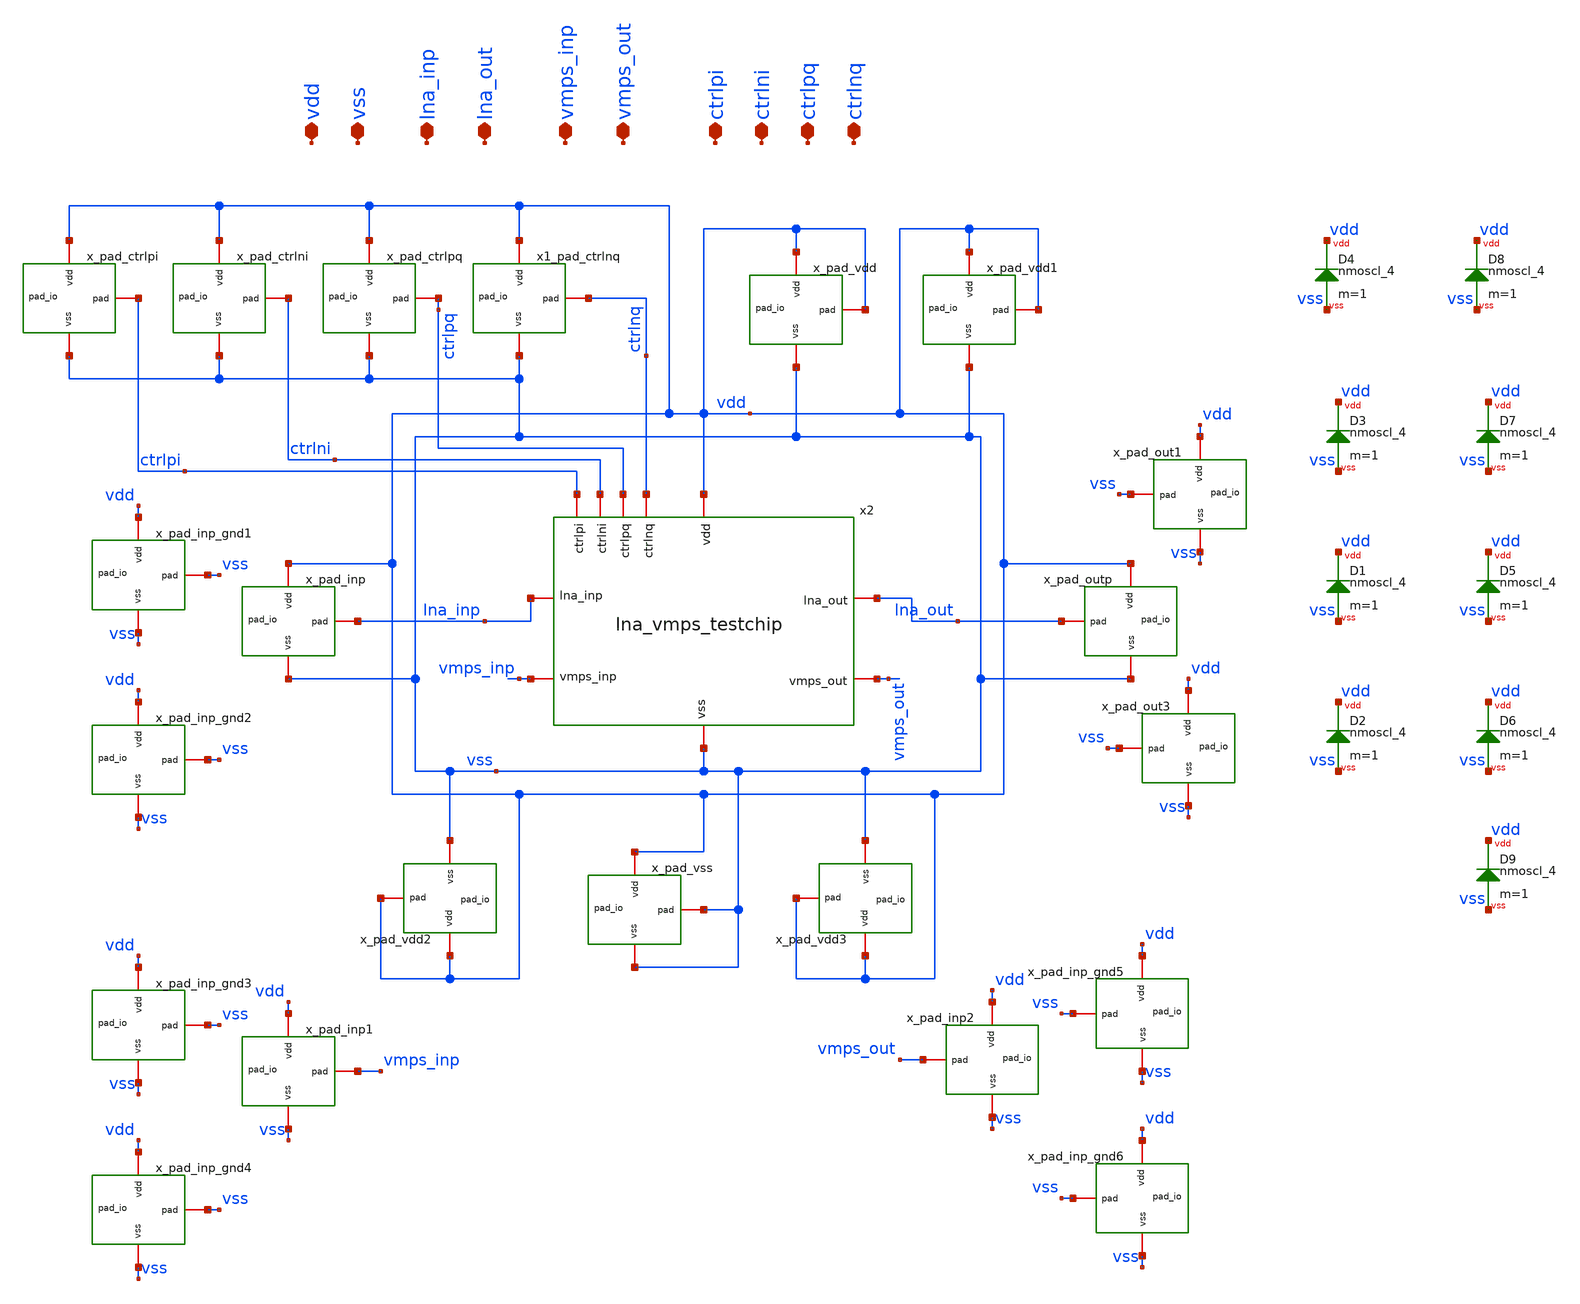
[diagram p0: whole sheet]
** sch_path: LNA7096-main/schematic/xschem/06_integ/top_lna_vmps_testchip.sch
**.subckt top_lna_vmps_testchip vdd vss lna_inp lna_out ctrlpi ctrlni ctrlpq ctrlnq vmps_inp
*+ vmps_out
*.iopin vdd
*.iopin vss
*.iopin lna_inp
*.iopin lna_out
*.iopin ctrlpi
*.iopin ctrlni
*.iopin ctrlpq
*.iopin ctrlnq
*.iopin vmps_inp
*.iopin vmps_out
x_pad_inp vdd lna_inp vss pad_io
x_pad_vss vdd vss vss pad_io
x_pad_outp vdd lna_out vss pad_io
x_pad_vdd vdd vdd vss pad_io
x_pad_ctrlpi vdd ctrlpi vss pad_io
x_pad_ctrlni vdd ctrlni vss pad_io
x_pad_ctrlpq vdd ctrlpq vss pad_io
x1_pad_ctrlnq vdd ctrlnq vss pad_io
x_pad_inp_gnd1 vdd vss vss pad_io
x_pad_inp_gnd2 vdd vss vss pad_io
x_pad_out1 vdd vss vss pad_io
x_pad_out3 vdd vss vss pad_io
x_pad_vdd1 vdd vdd vss pad_io
XD1 vdd vss nmoscl_4 m=1
XD2 vdd vss nmoscl_4 m=1
XD3 vdd vss nmoscl_4 m=1
XD4 vdd vss nmoscl_4 m=1
XD5 vdd vss nmoscl_4 m=1
XD6 vdd vss nmoscl_4 m=1
XD7 vdd vss nmoscl_4 m=1
XD8 vdd vss nmoscl_4 m=1
XD9 vdd vss nmoscl_4 m=1
x_pad_inp1 vdd vmps_inp vss pad_io
x_pad_inp_gnd3 vdd vss vss pad_io
x_pad_inp_gnd4 vdd vss vss pad_io
x_pad_inp2 vdd vmps_out vss pad_io
x_pad_inp_gnd5 vdd vss vss pad_io
x_pad_inp_gnd6 vdd vss vss pad_io
x_pad_vdd2 vdd vdd vss pad_io
x_pad_vdd3 vdd vdd vss pad_io
x2 lna_inp vmps_out vmps_inp lna_out vdd ctrlpi ctrlpq ctrlnq ctrlni vss lna_vmps_testchip
**.ends
.end
